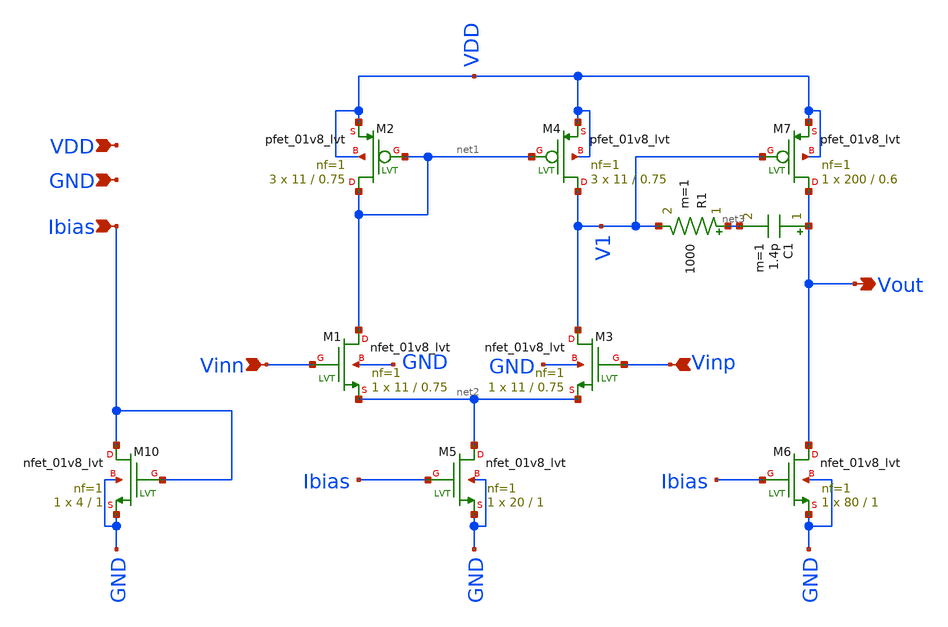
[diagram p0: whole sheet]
** sch_path: single_ended_ota.sch
**.subckt single_ended_ota Vout Vinn Vinp Ibias VDD GND
*.opin Vout
*.ipin Vinn
*.ipin Vinp
*.ipin Ibias
*.ipin VDD
*.ipin GND
XM1 net1 Vinn net2 GND sky130_fd_pr__nfet_01v8_lvt L=0.75 W=11 nf=1 ad='int((nf+1)/2) * W/nf * 0.29'
+ as='int((nf+2)/2) * W/nf * 0.29' pd='2*int((nf+1)/2) * (W/nf + 0.29)' ps='2*int((nf+2)/2) * (W/nf + 0.29)'
+ nrd='0.29 / W' nrs='0.29 / W' sa=0 sb=0 sd=0 mult=1 m=1
XM2 net1 net1 VDD VDD sky130_fd_pr__pfet_01v8_lvt L=0.75 W=11 nf=1 ad='int((nf+1)/2) * W/nf * 0.29' as='int((nf+2)/2) * W/nf * 0.29'
+ pd='2*int((nf+1)/2) * (W/nf + 0.29)' ps='2*int((nf+2)/2) * (W/nf + 0.29)' nrd='0.29 / W' nrs='0.29 / W'
+ sa=0 sb=0 sd=0 mult=3 m=3
XM3 V1 Vinp net2 GND sky130_fd_pr__nfet_01v8_lvt L=0.75 W=11 nf=1 ad='int((nf+1)/2) * W/nf * 0.29' as='int((nf+2)/2) * W/nf * 0.29'
+ pd='2*int((nf+1)/2) * (W/nf + 0.29)' ps='2*int((nf+2)/2) * (W/nf + 0.29)' nrd='0.29 / W' nrs='0.29 / W'
+ sa=0 sb=0 sd=0 mult=1 m=1
XM4 V1 net1 VDD VDD sky130_fd_pr__pfet_01v8_lvt L=0.75 W=11 nf=1 ad='int((nf+1)/2) * W/nf * 0.29' as='int((nf+2)/2) * W/nf * 0.29'
+ pd='2*int((nf+1)/2) * (W/nf + 0.29)' ps='2*int((nf+2)/2) * (W/nf + 0.29)' nrd='0.29 / W' nrs='0.29 / W'
+ sa=0 sb=0 sd=0 mult=3 m=3
XM5 net2 Ibias GND GND sky130_fd_pr__nfet_01v8_lvt L=1 W=20 nf=1 ad='int((nf+1)/2) * W/nf * 0.29' as='int((nf+2)/2) * W/nf * 0.29'
+ pd='2*int((nf+1)/2) * (W/nf + 0.29)' ps='2*int((nf+2)/2) * (W/nf + 0.29)' nrd='0.29 / W' nrs='0.29 / W'
+ sa=0 sb=0 sd=0 mult=1 m=1
XM6 Vout Ibias GND GND sky130_fd_pr__nfet_01v8_lvt L=1 W=80 nf=1 ad='int((nf+1)/2) * W/nf * 0.29' as='int((nf+2)/2) * W/nf * 0.29'
+ pd='2*int((nf+1)/2) * (W/nf + 0.29)' ps='2*int((nf+2)/2) * (W/nf + 0.29)' nrd='0.29 / W' nrs='0.29 / W'
+ sa=0 sb=0 sd=0 mult=1 m=1
XM7 Vout V1 VDD VDD sky130_fd_pr__pfet_01v8_lvt L=0.6 W=200 nf=1 ad='int((nf+1)/2) * W/nf * 0.29' as='int((nf+2)/2) * W/nf * 0.29'
+ pd='2*int((nf+1)/2) * (W/nf + 0.29)' ps='2*int((nf+2)/2) * (W/nf + 0.29)' nrd='0.29 / W' nrs='0.29 / W'
+ sa=0 sb=0 sd=0 mult=1 m=1
R1 net3 V1 1000 m=1
C1 Vout net3 1.4p m=1
XM10 Ibias Ibias GND GND sky130_fd_pr__nfet_01v8_lvt L=1 W=4 nf=1 ad='int((nf+1)/2) * W/nf * 0.29' as='int((nf+2)/2) * W/nf * 0.29'
+ pd='2*int((nf+1)/2) * (W/nf + 0.29)' ps='2*int((nf+2)/2) * (W/nf + 0.29)' nrd='0.29 / W' nrs='0.29 / W'
+ sa=0 sb=0 sd=0 mult=1 m=1
**.ends
.end
